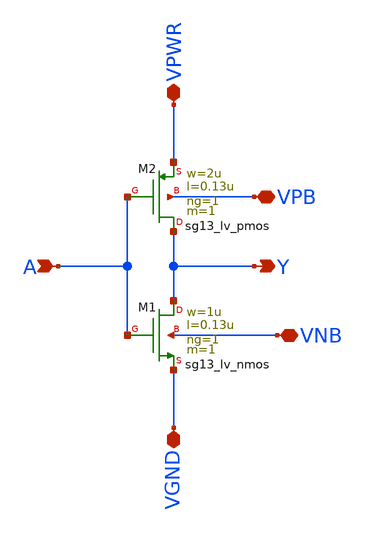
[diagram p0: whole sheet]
** sch_path: 30_MHz_Fractional_N_PLL/design_data/xschem/VCO_INV.sch
**.subckt VCO_INV VPWR VGND A Y VPB VNB
*.iopin VPWR
*.iopin VGND
*.ipin A
*.opin Y
*.iopin VPB
*.iopin VNB
XM2 Y A VPWR VPB sg13_lv_pmos w=2u l=0.13u ng=1 m=1 mm_ok=1
XM1 Y A VGND VNB sg13_lv_nmos w=1u l=0.13u ng=1 m=1 mm_ok=1
**.ends
.end
